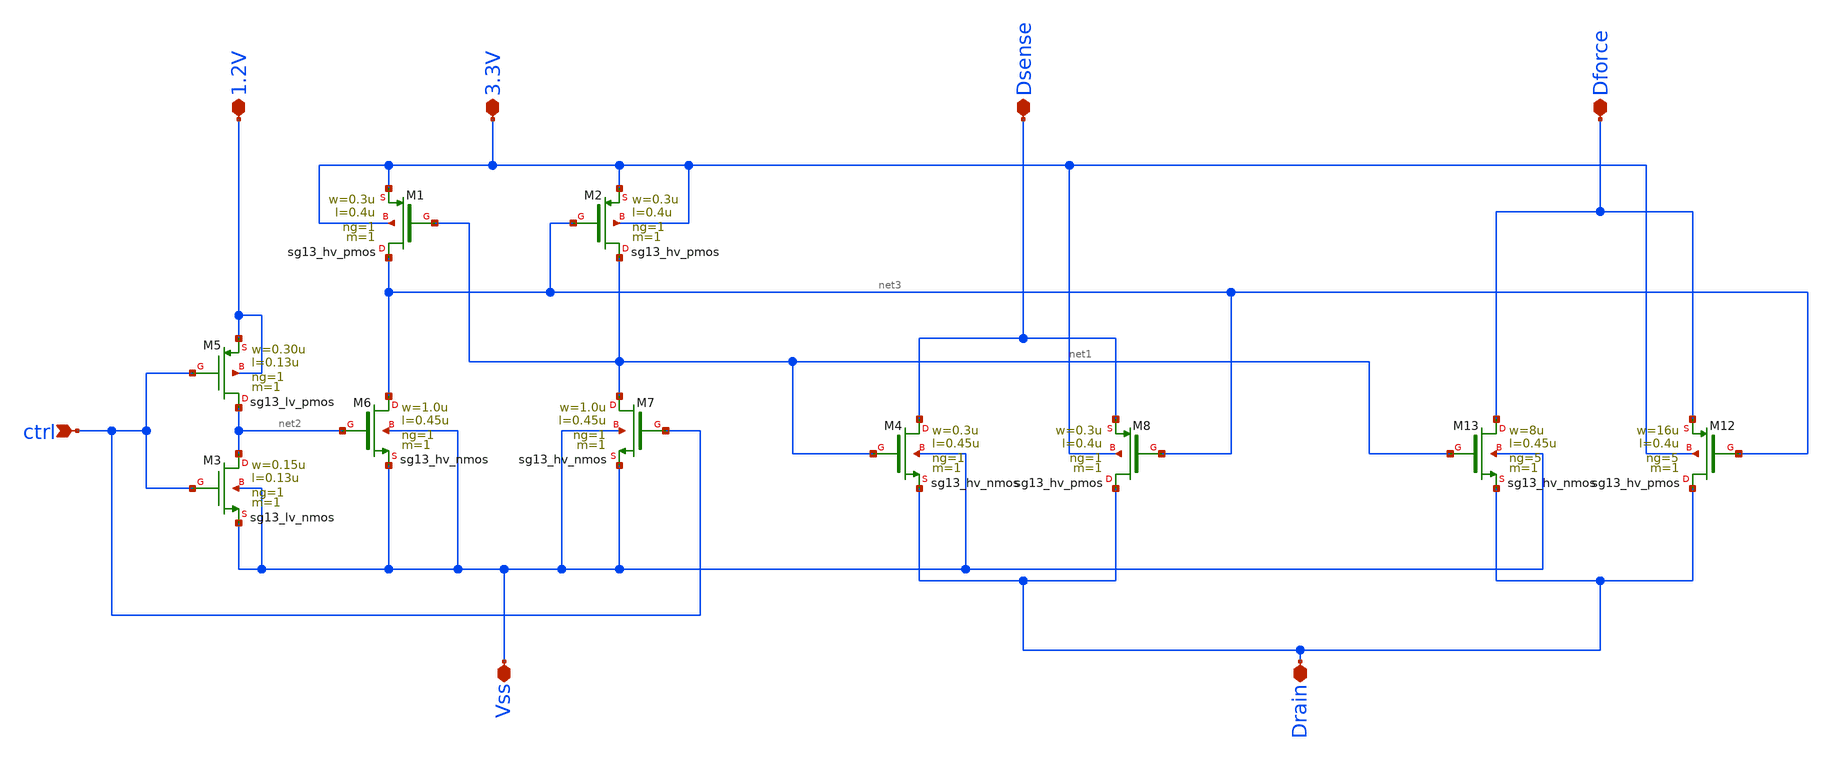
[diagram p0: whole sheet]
** sch_path: design_data/xschem/level_shifter_ver.sch
* Copyright 2025 IHP PDK Authors
**.subckt level_shifter_ver Vss 3.3V ctrl 1.2V Dsense Drain Dforce
*.iopin Vss
*.iopin 3.3V
*.ipin ctrl
*.iopin 1.2V
*.iopin Dsense
*.iopin Drain
*.iopin Dforce
XM2 net1 net3 3.3V 3.3V sg13_hv_pmos w=0.3u l=0.4u ng=1 m=1 mm_ok=1
XM3 net2 ctrl Vss Vss sg13_lv_nmos w=0.15u l=0.13u ng=1 m=1 mm_ok=1
XM5 net2 ctrl 1.2V 1.2V sg13_lv_pmos w=0.30u l=0.13u ng=1 m=1 mm_ok=1
XM1 net3 net1 3.3V 3.3V sg13_hv_pmos w=0.3u l=0.4u ng=1 m=1 mm_ok=1
XM6 net3 net2 Vss Vss sg13_hv_nmos w=1.0u l=0.45u ng=1 m=1 mm_ok=1
XM7 net1 ctrl Vss Vss sg13_hv_nmos w=1.0u l=0.45u ng=1 m=1 mm_ok=1
XM12 Drain net3 Dforce 3.3V sg13_hv_pmos w=16u l=0.4u ng=5 m=1 mm_ok=1
XM13 Dforce net1 Drain Vss sg13_hv_nmos w=8u l=0.45u ng=5 m=1 mm_ok=1
XM4 Dsense net1 Drain Vss sg13_hv_nmos w=0.3u l=0.45u ng=1 m=1 mm_ok=1
XM8 Drain net3 Dsense 3.3V sg13_hv_pmos w=0.3u l=0.4u ng=1 m=1 mm_ok=1
**.ends
.end
